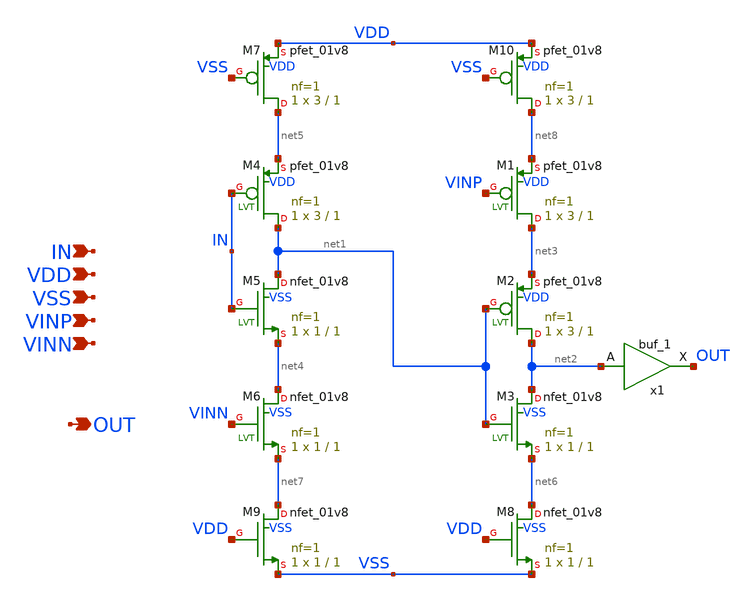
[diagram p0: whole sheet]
** sch_path: xschem/delay_gate.sch
**.subckt delay_gate VINP VINN IN VSS VDD OUT
*.ipin VINP
*.ipin VINN
*.ipin IN
*.ipin VSS
*.ipin VDD
*.opin OUT
XM1 net3 VINP net8 VDD sky130_fd_pr__pfet_01v8 L=1 W=3 nf=1 ad='int((nf+1)/2) * W/nf * 0.29' as='int((nf+2)/2) * W/nf * 0.29'
+ pd='2*int((nf+1)/2) * (W/nf + 0.29)' ps='2*int((nf+2)/2) * (W/nf + 0.29)' nrd='0.29 / W' nrs='0.29 / W'
+ sa=0 sb=0 sd=0 mult=1 m=1
XM2 net2 net1 net3 VDD sky130_fd_pr__pfet_01v8 L=1 W=3 nf=1 ad='int((nf+1)/2) * W/nf * 0.29' as='int((nf+2)/2) * W/nf * 0.29'
+ pd='2*int((nf+1)/2) * (W/nf + 0.29)' ps='2*int((nf+2)/2) * (W/nf + 0.29)' nrd='0.29 / W' nrs='0.29 / W'
+ sa=0 sb=0 sd=0 mult=1 m=1
XM3 net2 net1 net6 VSS sky130_fd_pr__nfet_01v8 L=1 W=1 nf=1 ad='int((nf+1)/2) * W/nf * 0.29' as='int((nf+2)/2) * W/nf * 0.29'
+ pd='2*int((nf+1)/2) * (W/nf + 0.29)' ps='2*int((nf+2)/2) * (W/nf + 0.29)' nrd='0.29 / W' nrs='0.29 / W'
+ sa=0 sb=0 sd=0 mult=1 m=1
XM4 net1 IN net5 VDD sky130_fd_pr__pfet_01v8 L=1 W=3 nf=1 ad='int((nf+1)/2) * W/nf * 0.29' as='int((nf+2)/2) * W/nf * 0.29'
+ pd='2*int((nf+1)/2) * (W/nf + 0.29)' ps='2*int((nf+2)/2) * (W/nf + 0.29)' nrd='0.29 / W' nrs='0.29 / W'
+ sa=0 sb=0 sd=0 mult=1 m=1
XM5 net1 IN net4 VSS sky130_fd_pr__nfet_01v8 L=1 W=1 nf=1 ad='int((nf+1)/2) * W/nf * 0.29' as='int((nf+2)/2) * W/nf * 0.29'
+ pd='2*int((nf+1)/2) * (W/nf + 0.29)' ps='2*int((nf+2)/2) * (W/nf + 0.29)' nrd='0.29 / W' nrs='0.29 / W'
+ sa=0 sb=0 sd=0 mult=1 m=1
XM6 net4 VINN net7 VSS sky130_fd_pr__nfet_01v8 L=1 W=1 nf=1 ad='int((nf+1)/2) * W/nf * 0.29' as='int((nf+2)/2) * W/nf * 0.29'
+ pd='2*int((nf+1)/2) * (W/nf + 0.29)' ps='2*int((nf+2)/2) * (W/nf + 0.29)' nrd='0.29 / W' nrs='0.29 / W'
+ sa=0 sb=0 sd=0 mult=1 m=1
XM7 net5 VSS VDD VDD sky130_fd_pr__pfet_01v8 L=1 W=3 nf=1 ad='int((nf+1)/2) * W/nf * 0.29' as='int((nf+2)/2) * W/nf * 0.29'
+ pd='2*int((nf+1)/2) * (W/nf + 0.29)' ps='2*int((nf+2)/2) * (W/nf + 0.29)' nrd='0.29 / W' nrs='0.29 / W'
+ sa=0 sb=0 sd=0 mult=1 m=1
XM8 net6 VDD VSS VSS sky130_fd_pr__nfet_01v8 L=1 W=1 nf=1 ad='int((nf+1)/2) * W/nf * 0.29' as='int((nf+2)/2) * W/nf * 0.29'
+ pd='2*int((nf+1)/2) * (W/nf + 0.29)' ps='2*int((nf+2)/2) * (W/nf + 0.29)' nrd='0.29 / W' nrs='0.29 / W'
+ sa=0 sb=0 sd=0 mult=1 m=1
XM9 net7 VDD VSS VSS sky130_fd_pr__nfet_01v8 L=1 W=1 nf=1 ad='int((nf+1)/2) * W/nf * 0.29' as='int((nf+2)/2) * W/nf * 0.29'
+ pd='2*int((nf+1)/2) * (W/nf + 0.29)' ps='2*int((nf+2)/2) * (W/nf + 0.29)' nrd='0.29 / W' nrs='0.29 / W'
+ sa=0 sb=0 sd=0 mult=1 m=1
XM10 net8 VSS VDD VDD sky130_fd_pr__pfet_01v8 L=1 W=3 nf=1 ad='int((nf+1)/2) * W/nf * 0.29' as='int((nf+2)/2) * W/nf * 0.29'
+ pd='2*int((nf+1)/2) * (W/nf + 0.29)' ps='2*int((nf+2)/2) * (W/nf + 0.29)' nrd='0.29 / W' nrs='0.29 / W'
+ sa=0 sb=0 sd=0 mult=1 m=1
x1 net2 VGND VNB VPB VPWR OUT sky130_fd_sc_hs__buf_1
**.ends
.end
